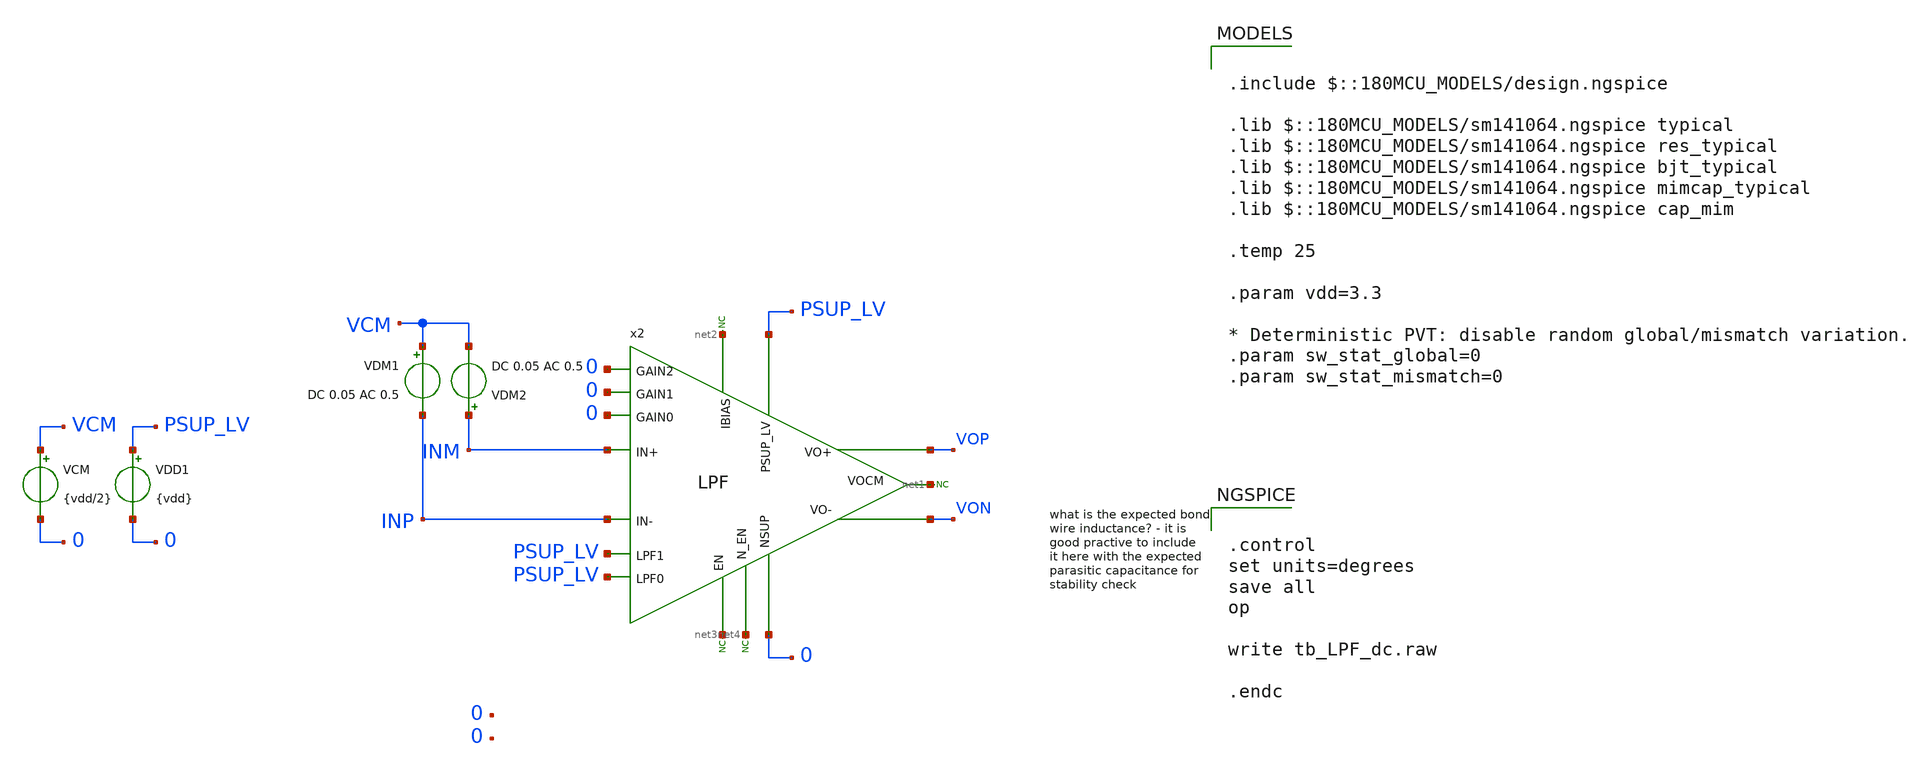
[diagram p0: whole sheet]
** sch_path: xschem/blocks/LPF/tb_LPF_dc.sch
**.subckt tb_LPF_dc
VDD1 PSUP_LV 0 {vdd}
VCM VCM 0 {vdd/2}
* noconn #net1
* noconn #net2
* noconn #net3
* noconn #net4
VDM2 INM VCM DC 0.05 AC 0.5
VDM1 VCM INP DC 0.05 AC 0.5
x2 PSUP_LV 0 net3 net4 net2 0 0 0 PSUP_LV PSUP_LV INM VOP net1 INP VON LPF
**** begin user architecture code

.include $::180MCU_MODELS/design.ngspice

.lib $::180MCU_MODELS/sm141064.ngspice typical
.lib $::180MCU_MODELS/sm141064.ngspice res_typical
.lib $::180MCU_MODELS/sm141064.ngspice bjt_typical
.lib $::180MCU_MODELS/sm141064.ngspice mimcap_typical
.lib $::180MCU_MODELS/sm141064.ngspice cap_mim

.temp 25

.param vdd=3.3

* Deterministic PVT: disable random global/mismatch variation.
.param sw_stat_global=0
.param sw_stat_mismatch=0



.control
set units=degrees
save all
op

write tb_LPF_dc.raw

.endc


**** end user architecture code
**.ends
.end
